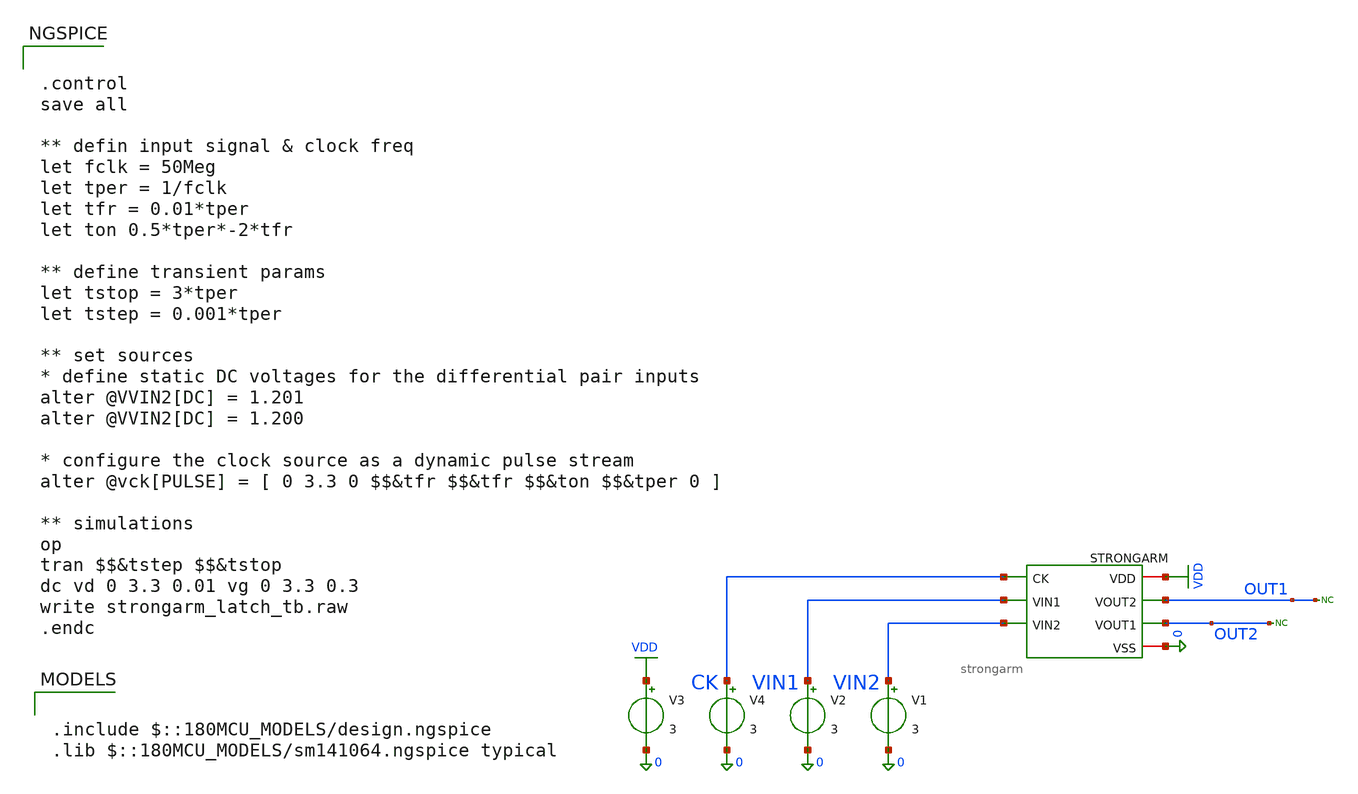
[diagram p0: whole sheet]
** sch_path: comparator/schematic/backup_files/strongarm_tb_backup.sch
**.subckt strongarm_tb_backup
STRONGARM VDD CK OUT1 OUT2 VIN1 VIN2 0 strongarm
V1 VIN2 0 3
V2 VIN1 0 3
V3 VDD 0 3
V4 CK 0 3
* noconn OUT2
* noconn OUT1
**** begin user architecture code

.include $::180MCU_MODELS/design.ngspice
.lib $::180MCU_MODELS/sm141064.ngspice typical



.control
save all

** defin input signal & clock freq
let fclk = 50Meg
let tper = 1/fclk
let tfr = 0.01*tper
let ton 0.5*tper*-2*tfr

** define transient params
let tstop = 3*tper
let tstep = 0.001*tper

** set sources
* define static DC voltages for the differential pair inputs
alter @VVIN2[DC] = 1.201
alter @VVIN2[DC] = 1.200

* configure the clock source as a dynamic pulse stream
alter @vck[PULSE] = [ 0 3.3 0 $$&tfr $$&tfr $$&ton $$&tper 0 ]

** simulations
op
tran $$&tstep $$&tstop
dc vd 0 3.3 0.01 vg 0 3.3 0.3
write strongarm_latch_tb.raw
.endc


**** end user architecture code
**.ends

* expanding   symbol:  comparator/schematic/strongarm.sym # of pins=7
** sym_path: comparator/schematic/strongarm.sym
** sch_path: comparator/schematic/strongarm.sch
.subckt strongarm VDD CK VOUT2 VOUT1 VIN1 VIN2 VSS
*.opin VOUT1
*.opin VOUT2
*.ipin VIN1
*.ipin VIN2
*.ipin CK
*.iopin VDD
*.iopin VSS
XM1 VOUT2 VOUT1 net1 net1 nfet_03v3 L=0.28u W=0.22u nf=1 ad='int((nf+1)/2) * W/nf * 0.18u' as='int((nf+2)/2) * W/nf * 0.18u'
+ pd='2*int((nf+1)/2) * (W/nf + 0.18u)' ps='2*int((nf+2)/2) * (W/nf + 0.18u)' nrd='0.18u / W' nrs='0.18u / W'
+ sa=0 sb=0 sd=0 m=1
XM2 VOUT1 VOUT2 VDD VDD pfet_03v3 L=0.28u W=0.22u nf=1 ad='int((nf+1)/2) * W/nf * 0.18u' as='int((nf+2)/2) * W/nf * 0.18u'
+ pd='2*int((nf+1)/2) * (W/nf + 0.18u)' ps='2*int((nf+2)/2) * (W/nf + 0.18u)' nrd='0.18u / W' nrs='0.18u / W'
+ sa=0 sb=0 sd=0 m=1
XM3 VOUT1 CK VDD VDD pfet_03v3 L=0.28u W=0.22u nf=1 ad='int((nf+1)/2) * W/nf * 0.18u' as='int((nf+2)/2) * W/nf * 0.18u'
+ pd='2*int((nf+1)/2) * (W/nf + 0.18u)' ps='2*int((nf+2)/2) * (W/nf + 0.18u)' nrd='0.18u / W' nrs='0.18u / W'
+ sa=0 sb=0 sd=0 m=1
XM4 net3 CK VDD VDD pfet_03v3 L=0.28u W=0.22u nf=1 ad='int((nf+1)/2) * W/nf * 0.18u' as='int((nf+2)/2) * W/nf * 0.18u'
+ pd='2*int((nf+1)/2) * (W/nf + 0.18u)' ps='2*int((nf+2)/2) * (W/nf + 0.18u)' nrd='0.18u / W' nrs='0.18u / W'
+ sa=0 sb=0 sd=0 m=1
XM5 net1 CK VDD VDD pfet_03v3 L=0.28u W=0.22u nf=1 ad='int((nf+1)/2) * W/nf * 0.18u' as='int((nf+2)/2) * W/nf * 0.18u'
+ pd='2*int((nf+1)/2) * (W/nf + 0.18u)' ps='2*int((nf+2)/2) * (W/nf + 0.18u)' nrd='0.18u / W' nrs='0.18u / W'
+ sa=0 sb=0 sd=0 m=1
XM6 VOUT2 CK VDD VDD pfet_03v3 L=0.28u W=0.22u nf=1 ad='int((nf+1)/2) * W/nf * 0.18u' as='int((nf+2)/2) * W/nf * 0.18u'
+ pd='2*int((nf+1)/2) * (W/nf + 0.18u)' ps='2*int((nf+2)/2) * (W/nf + 0.18u)' nrd='0.18u / W' nrs='0.18u / W'
+ sa=0 sb=0 sd=0 m=1
XM7 VOUT2 VOUT1 VDD VDD pfet_03v3 L=0.28u W=0.22u nf=1 ad='int((nf+1)/2) * W/nf * 0.18u' as='int((nf+2)/2) * W/nf * 0.18u'
+ pd='2*int((nf+1)/2) * (W/nf + 0.18u)' ps='2*int((nf+2)/2) * (W/nf + 0.18u)' nrd='0.18u / W' nrs='0.18u / W'
+ sa=0 sb=0 sd=0 m=1
XM8 net1 VIN2 net2 net2 nfet_03v3 L=0.28u W=0.22u nf=1 ad='int((nf+1)/2) * W/nf * 0.18u' as='int((nf+2)/2) * W/nf * 0.18u'
+ pd='2*int((nf+1)/2) * (W/nf + 0.18u)' ps='2*int((nf+2)/2) * (W/nf + 0.18u)' nrd='0.18u / W' nrs='0.18u / W'
+ sa=0 sb=0 sd=0 m=1
XM9 VOUT1 VOUT2 net3 net3 nfet_03v3 L=0.28u W=0.22u nf=1 ad='int((nf+1)/2) * W/nf * 0.18u' as='int((nf+2)/2) * W/nf * 0.18u'
+ pd='2*int((nf+1)/2) * (W/nf + 0.18u)' ps='2*int((nf+2)/2) * (W/nf + 0.18u)' nrd='0.18u / W' nrs='0.18u / W'
+ sa=0 sb=0 sd=0 m=1
XM10 net3 VIN1 net2 net2 nfet_03v3 L=0.28u W=0.22u nf=1 ad='int((nf+1)/2) * W/nf * 0.18u' as='int((nf+2)/2) * W/nf * 0.18u'
+ pd='2*int((nf+1)/2) * (W/nf + 0.18u)' ps='2*int((nf+2)/2) * (W/nf + 0.18u)' nrd='0.18u / W' nrs='0.18u / W'
+ sa=0 sb=0 sd=0 m=1
XM11 net2 CK VSS net2 nfet_03v3 L=0.28u W=0.22u nf=1 ad='int((nf+1)/2) * W/nf * 0.18u' as='int((nf+2)/2) * W/nf * 0.18u'
+ pd='2*int((nf+1)/2) * (W/nf + 0.18u)' ps='2*int((nf+2)/2) * (W/nf + 0.18u)' nrd='0.18u / W' nrs='0.18u / W'
+ sa=0 sb=0 sd=0 m=1
.ends

.GLOBAL VDD
.end
